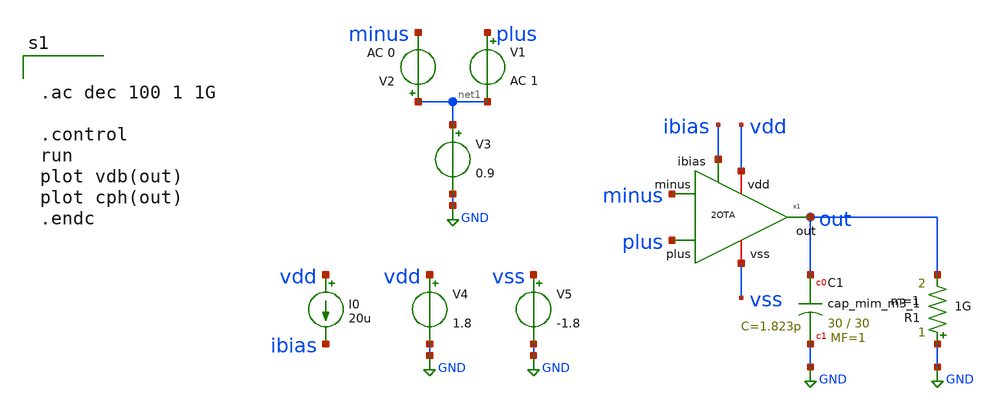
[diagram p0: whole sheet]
** sch_path: 2OTA_tb_gbw_post.sch
**.subckt 2OTA_tb_gbw_post
V1 plus net1 AC 1
V2 net1 minus AC 0
V3 net1 GND 0.9
V4 vdd GND 1.8
V5 vss GND -1.8
I0 vdd ibias 20u
x1 vdd plus out minus ibias vss 2OTA
XC1 out GND sky130_fd_pr__cap_mim_m3_1 W=30 L=30 MF=1 m=1
R1 GND out 1G m=1
**** begin user architecture code


.ac dec 100 1 1G

.control
run
plot vdb(out)
plot cph(out)
.endc



** opencircuitdesign pdks install
.lib $::SKYWATER_MODELS/sky130.lib.spice tt
.include /foss/designs/dsrt/dsrt_proj/2OTA_pex.spice

**** end user architecture code
**.ends

* expanding   symbol:  2OTA.sym # of pins=6
** sym_path: 2OTA.sym
** sch_path: 2OTA.sch
.subckt 2OTA vdd plus out minus ibias vss
*.ipin ibias
*.ipin minus
*.ipin plus
*.iopin vdd
*.iopin vss
*.opin out
XM1 net2 net1 vdd vdd sky130_fd_pr__pfet_01v8 L=1 W=1.5 nf=1 ad='int((1 + 1)/2) * 1.5 / 1 * 0.29' as='int((1 + 2)/2) * 1.5 / 1 * 0.29'
+ pd='2*int((1 + 1)/2) * (1.5 / 1 + 0.29)' ps='2*int((1 + 2)/2) * (1.5 / 1 + 0.29)' nrd='0.29 / 1.5 ' nrs='0.29 / 1.5 '
+ sa=0 sb=0 sd=0 mult=1 m=1
XM2 net1 net1 vdd vdd sky130_fd_pr__pfet_01v8 L=1 W=1.5 nf=1 ad='int((1 + 1)/2) * 1.5 / 1 * 0.29' as='int((1 + 2)/2) * 1.5 / 1 * 0.29'
+ pd='2*int((1 + 1)/2) * (1.5 / 1 + 0.29)' ps='2*int((1 + 2)/2) * (1.5 / 1 + 0.29)' nrd='0.29 / 1.5 ' nrs='0.29 / 1.5 '
+ sa=0 sb=0 sd=0 mult=1 m=1
XM3 net1 minus net3 vss sky130_fd_pr__nfet_01v8 L=1 W=1.5 nf=1 ad='int((1 + 1)/2) * 1.5 / 1 * 0.29' as='int((1 + 2)/2) * 1.5 / 1 * 0.29'
+ pd='2*int((1 + 1)/2) * (1.5 / 1 + 0.29)' ps='2*int((1 + 2)/2) * (1.5 / 1 + 0.29)' nrd='0.29 / 1.5 ' nrs='0.29 / 1.5 '
+ sa=0 sb=0 sd=0 mult=1 m=1
XM4 net2 plus net3 vss sky130_fd_pr__nfet_01v8 L=1 W=1.5 nf=1 ad='int((1 + 1)/2) * 1.5 / 1 * 0.29' as='int((1 + 2)/2) * 1.5 / 1 * 0.29'
+ pd='2*int((1 + 1)/2) * (1.5 / 1 + 0.29)' ps='2*int((1 + 2)/2) * (1.5 / 1 + 0.29)' nrd='0.29 / 1.5 ' nrs='0.29 / 1.5 '
+ sa=0 sb=0 sd=0 mult=1 m=1
XM5 ibias ibias vss vss sky130_fd_pr__nfet_01v8 L=1 W=1.5 nf=1 ad='int((1 + 1)/2) * 1.5 / 1 * 0.29' as='int((1 + 2)/2) * 1.5 / 1 * 0.29'
+ pd='2*int((1 + 1)/2) * (1.5 / 1 + 0.29)' ps='2*int((1 + 2)/2) * (1.5 / 1 + 0.29)' nrd='0.29 / 1.5 ' nrs='0.29 / 1.5 '
+ sa=0 sb=0 sd=0 mult=1 m=1
XM6 net3 ibias vss vss sky130_fd_pr__nfet_01v8 L=1 W=1.5 nf=1 ad='int((1 + 1)/2) * 1.5 / 1 * 0.29' as='int((1 + 2)/2) * 1.5 / 1 * 0.29'
+ pd='2*int((1 + 1)/2) * (1.5 / 1 + 0.29)' ps='2*int((1 + 2)/2) * (1.5 / 1 + 0.29)' nrd='0.29 / 1.5 ' nrs='0.29 / 1.5 '
+ sa=0 sb=0 sd=0 mult=1 m=1
XM7 out net2 vdd vdd sky130_fd_pr__pfet_01v8 L=1 W=34 nf=4 ad='int((4 + 1)/2) * 34 / 4 * 0.29' as='int((4 + 2)/2) * 34 / 4 * 0.29'
+ pd='2*int((4 + 1)/2) * (34 / 4 + 0.29)' ps='2*int((4 + 2)/2) * (34 / 4 + 0.29)' nrd='0.29 / 34 ' nrs='0.29 / 34 '
+ sa=0 sb=0 sd=0 mult=1 m=1
XM8 out ibias vss vss sky130_fd_pr__nfet_01v8 L=1 W=13 nf=2 ad='int((2 + 1)/2) * 13 / 2 * 0.29' as='int((2 + 2)/2) * 13 / 2 * 0.29'
+ pd='2*int((2 + 1)/2) * (13 / 2 + 0.29)' ps='2*int((2 + 2)/2) * (13 / 2 + 0.29)' nrd='0.29 / 13 ' nrs='0.29 / 13 '
+ sa=0 sb=0 sd=0 mult=1 m=1
XC1 out net2 sky130_fd_pr__cap_mim_m3_1 W=7.5 L=7.5 MF=2 m=2
XC2 out net2 sky130_fd_pr__cap_mim_m3_1 W=7.5 L=7.5 MF=2 m=2
.ends

.GLOBAL GND
.end
